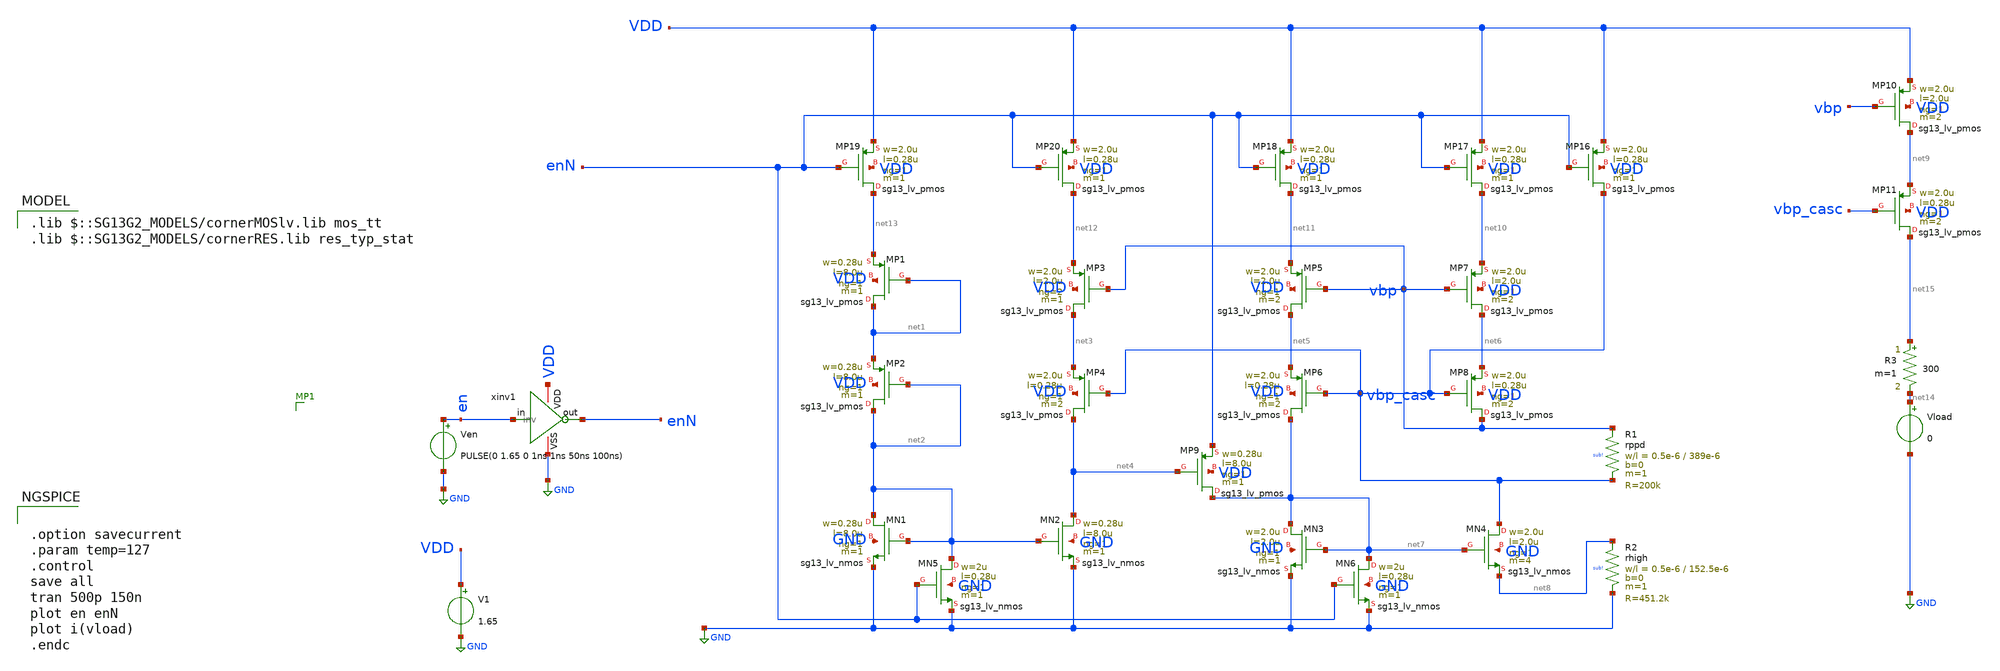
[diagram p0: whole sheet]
** sch_path: blocks/composite/dpi_adexp_neuron/design_data/xschem/trimmer.sch
**.subckt trimmer
XMP1 net1 net1 net13 VDD sg13_lv_pmos w=0.28u l=8.0u ng=1 m=1 mm_ok=1
XMP2 net2 net2 net1 VDD sg13_lv_pmos w=0.28u l=8.0u ng=1 m=1 mm_ok=1
XMN2 net4 net2 GND GND sg13_lv_nmos w=0.28u l=8.0u ng=1 m=1 mm_ok=1
XMN1 net2 net2 GND GND sg13_lv_nmos w=0.28u l=8.0u ng=1 m=1 mm_ok=1
XMP3 net3 vbp net12 VDD sg13_lv_pmos w=2.0u l=2.0u ng=2 m=1 mm_ok=1
XMP4 net4 vbp_casc net3 VDD sg13_lv_pmos w=2.0u l=0.28u ng=1 m=2 mm_ok=1
XMP5 net5 vbp net11 VDD sg13_lv_pmos w=2.0u l=2.0u ng=1 m=2 mm_ok=1
XMP6 net7 vbp_casc net5 VDD sg13_lv_pmos w=2.0u l=0.28u ng=1 m=2 mm_ok=1
XMP7 net6 vbp net10 VDD sg13_lv_pmos w=2.0u l=2.0u ng=1 m=2 mm_ok=1
XMP8 vbp vbp_casc net6 VDD sg13_lv_pmos w=2.0u l=0.28u ng=1 m=2 mm_ok=1
XMP9 net7 net4 enN VDD sg13_lv_pmos w=0.28u l=8.0u ng=1 m=1 mm_ok=1
XMN3 net7 net7 GND GND sg13_lv_nmos w=2.0u l=2.0u ng=1 m=1 mm_ok=1
XMN4 vbp_casc net7 net8 GND sg13_lv_nmos w=2.0u l=2.0u ng=1 m=4 mm_ok=1
XR1 vbp vbp_casc sub! rppd w=0.5e-6 l=389e-6 m=1 b=0 mm_ok=1
XR2 net8 GND sub! rhigh w=0.5e-6 l=152.5e-6 m=1 b=0 mm_ok=1
R3 net15 net14 300 m=1
XMP10 net9 vbp VDD VDD sg13_lv_pmos w=2.0u l=2.0u ng=1 m=2 mm_ok=1
XMP11 net15 vbp_casc net9 VDD sg13_lv_pmos w=2.0u l=0.28u ng=1 m=2 mm_ok=1
XMP16 vbp_casc enN VDD VDD sg13_lv_pmos w=2.0u l=0.28u ng=1 m=1 mm_ok=1
XMP17 net10 enN VDD VDD sg13_lv_pmos w=2.0u l=0.28u ng=1 m=1 mm_ok=1
XMP18 net11 enN VDD VDD sg13_lv_pmos w=2.0u l=0.28u ng=1 m=1 mm_ok=1
XMP19 net13 enN VDD VDD sg13_lv_pmos w=2.0u l=0.28u ng=1 m=1 mm_ok=1
XMP20 net12 enN VDD VDD sg13_lv_pmos w=2.0u l=0.28u ng=1 m=1 mm_ok=1
XMN5 net2 enN GND GND sg13_lv_nmos w=2u l=0.28u ng=1 m=1 mm_ok=1
XMN6 net7 enN GND GND sg13_lv_nmos w=2u l=0.28u ng=1 m=1 mm_ok=1
V1 VDD GND 1.65
Ven en GND PULSE(0 1.65 0 1ns 1ns 50ns 100ns)
xinv1 VDD en enN GND inv
Vload net14 GND 0
**** begin user architecture code


.option savecurrent
.param temp=127
.control
save all
tran 500p 150n
plot en enN
plot i(vload)
.endc


 .lib $::SG13G2_MODELS/cornerMOSlv.lib mos_tt
.lib $::SG13G2_MODELS/cornerRES.lib res_typ_stat

**** end user architecture code
**.ends

* expanding   symbol:  inv.sym # of pins=4
** sym_path: blocks/composite/dpi_adexp_neuron/design_data/xschem/dev/inv.sym
** sch_path: blocks/composite/dpi_adexp_neuron/design_data/xschem/dev/inv.sch
.subckt inv VDD in out VSS
*.iopin VDD
*.ipin in
*.iopin VSS
*.opin out
XM1 out in VSS VSS sg13_lv_nmos w=2.0u l=0.28u ng=1 m=1 mm_ok=1
XM2 out in VDD VDD sg13_lv_pmos w=2.0u l=0.28u ng=1 m=1 mm_ok=1
.ends

.GLOBAL GND
.end
